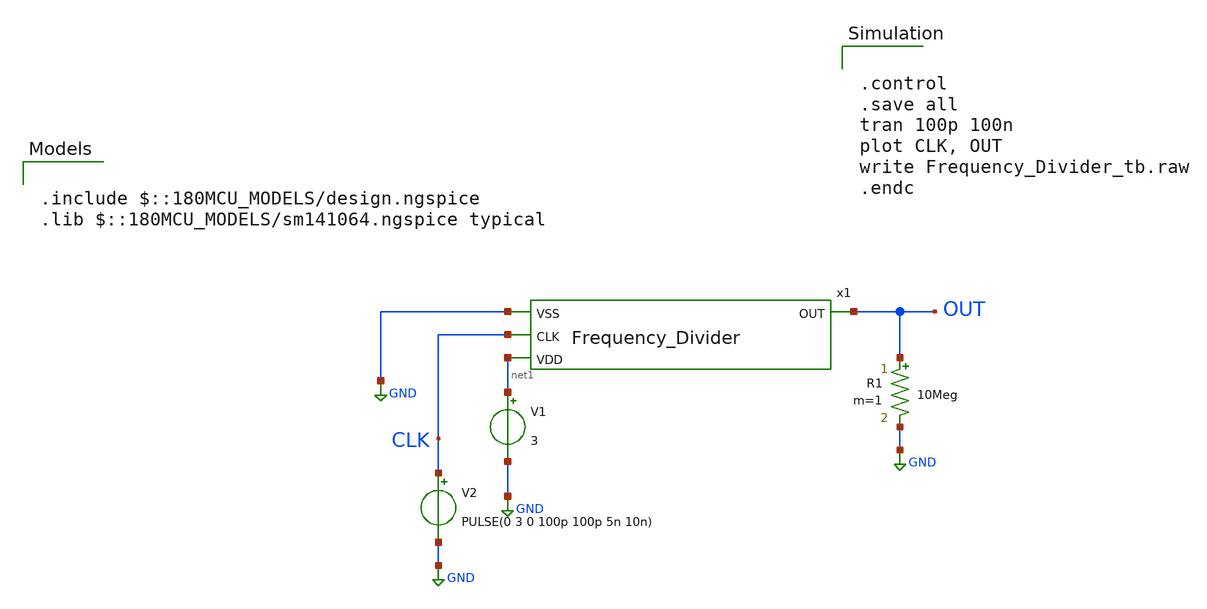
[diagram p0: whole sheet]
** sch_path: designs/libs/tb_analog/tb_frquency_divider/Frequency_Divider_tb.sch
**.subckt Frequency_Divider_tb
x1 GND OUT CLK net1 Frequency_Divider
V1 net1 GND 3
V2 CLK GND PULSE(0 3 0 100p 100p 5n 10n)
R1 OUT GND 10Meg m=1
**** begin user architecture code

.include $::180MCU_MODELS/design.ngspice
.lib $::180MCU_MODELS/sm141064.ngspice typical



.control
.save all
tran 100p 100n
plot CLK, OUT
write Frequency_Divider_tb.raw
.endc


**** end user architecture code
**.ends
.GLOBAL GND
.end
